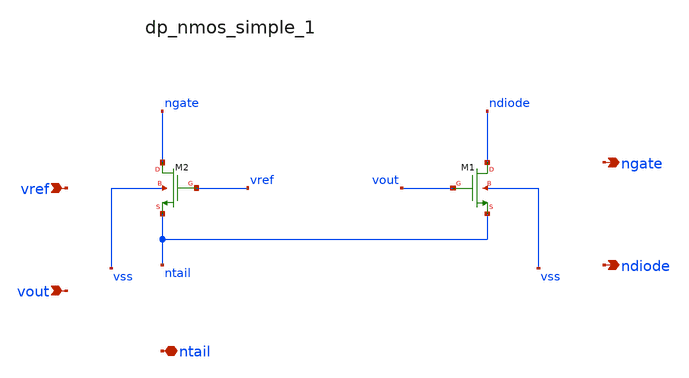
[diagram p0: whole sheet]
** sch_path: analog-db/raw/ldo_003_analoggym_simple/hier/blocks/dp_nmos_simple_1.sch
**.subckt dp_nmos_simple_1 vref vout ntail ngate ndiode
*.ipin vref
*.ipin vout
*.iopin ntail
*.opin ngate
*.opin ndiode
XM1 ndiode vout ntail vss sg13_hv_nmos w=x_dut_xm1_w l=x_dut_xm1_l ng=1 m=1
XM2 ngate vref ntail vss sg13_hv_nmos w=x_dut_xm2_w l=x_dut_xm2_l ng=1 m=1
**.ends
.end
